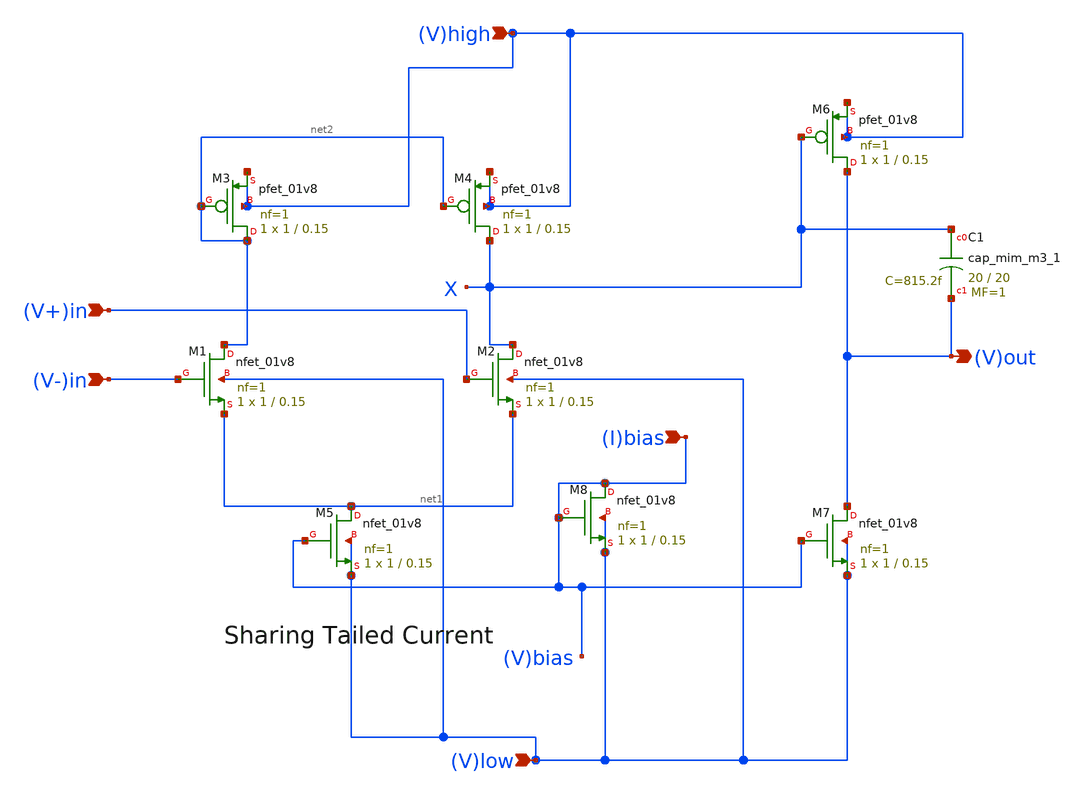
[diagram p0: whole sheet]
** sch_path: analog/bootcamp_opamp/schematics/opamp_two_stage.sch
**.subckt opamp_two_stage (V-)in (V+)in (V)out (I)bias (V)high (V)low
*.ipin (V-)in
*.ipin (V+)in
*.opin (V)out
*.ipin (I)bias
*.ipin (V)high
*.ipin (V)low
XM1 net2 (V-)in net1 (V)low sky130_fd_pr__nfet_01v8 L=0.15 W=1 nf=1 ad='int((nf+1)/2) * W/nf * 0.29'
+ as='int((nf+2)/2) * W/nf * 0.29' pd='2*int((nf+1)/2) * (W/nf + 0.29)' ps='2*int((nf+2)/2) * (W/nf + 0.29)'
+ nrd='0.29 / W' nrs='0.29 / W' sa=0 sb=0 sd=0 mult=1 m=1
XM2 X (V+)in net1 (V)low sky130_fd_pr__nfet_01v8 L=0.15 W=1 nf=1 ad='int((nf+1)/2) * W/nf * 0.29' as='int((nf+2)/2) * W/nf * 0.29'
+ pd='2*int((nf+1)/2) * (W/nf + 0.29)' ps='2*int((nf+2)/2) * (W/nf + 0.29)' nrd='0.29 / W' nrs='0.29 / W'
+ sa=0 sb=0 sd=0 mult=1 m=1
XM3 net2 net2 (V)high (V)high sky130_fd_pr__pfet_01v8 L=0.15 W=1 nf=1 ad='int((nf+1)/2) * W/nf * 0.29'
+ as='int((nf+2)/2) * W/nf * 0.29' pd='2*int((nf+1)/2) * (W/nf + 0.29)' ps='2*int((nf+2)/2) * (W/nf + 0.29)'
+ nrd='0.29 / W' nrs='0.29 / W' sa=0 sb=0 sd=0 mult=1 m=1
XM4 X net2 (V)high (V)high sky130_fd_pr__pfet_01v8 L=0.15 W=1 nf=1 ad='int((nf+1)/2) * W/nf * 0.29' as='int((nf+2)/2) * W/nf * 0.29'
+ pd='2*int((nf+1)/2) * (W/nf + 0.29)' ps='2*int((nf+2)/2) * (W/nf + 0.29)' nrd='0.29 / W' nrs='0.29 / W'
+ sa=0 sb=0 sd=0 mult=1 m=1
XM5 net1 (I)bias (V)low (V)low sky130_fd_pr__nfet_01v8 L=0.15 W=1 nf=1 ad='int((nf+1)/2) * W/nf * 0.29'
+ as='int((nf+2)/2) * W/nf * 0.29' pd='2*int((nf+1)/2) * (W/nf + 0.29)' ps='2*int((nf+2)/2) * (W/nf + 0.29)'
+ nrd='0.29 / W' nrs='0.29 / W' sa=0 sb=0 sd=0 mult=1 m=1
XM6 (V)out X (V)high (V)high sky130_fd_pr__pfet_01v8 L=0.15 W=1 nf=1 ad='int((nf+1)/2) * W/nf * 0.29'
+ as='int((nf+2)/2) * W/nf * 0.29' pd='2*int((nf+1)/2) * (W/nf + 0.29)' ps='2*int((nf+2)/2) * (W/nf + 0.29)'
+ nrd='0.29 / W' nrs='0.29 / W' sa=0 sb=0 sd=0 mult=1 m=1
XM7 (V)out (I)bias (V)low (V)low sky130_fd_pr__nfet_01v8 L=0.15 W=1 nf=1 ad='int((nf+1)/2) * W/nf * 0.29'
+ as='int((nf+2)/2) * W/nf * 0.29' pd='2*int((nf+1)/2) * (W/nf + 0.29)' ps='2*int((nf+2)/2) * (W/nf + 0.29)'
+ nrd='0.29 / W' nrs='0.29 / W' sa=0 sb=0 sd=0 mult=1 m=1
XM8 (I)bias (I)bias (V)low (V)low sky130_fd_pr__nfet_01v8 L=0.15 W=1 nf=1 ad='int((nf+1)/2) * W/nf * 0.29'
+ as='int((nf+2)/2) * W/nf * 0.29' pd='2*int((nf+1)/2) * (W/nf + 0.29)' ps='2*int((nf+2)/2) * (W/nf + 0.29)'
+ nrd='0.29 / W' nrs='0.29 / W' sa=0 sb=0 sd=0 mult=1 m=1
XC1 X (V)out sky130_fd_pr__cap_mim_m3_1 W=20 L=20 MF=1 m=1
**.ends
.end
